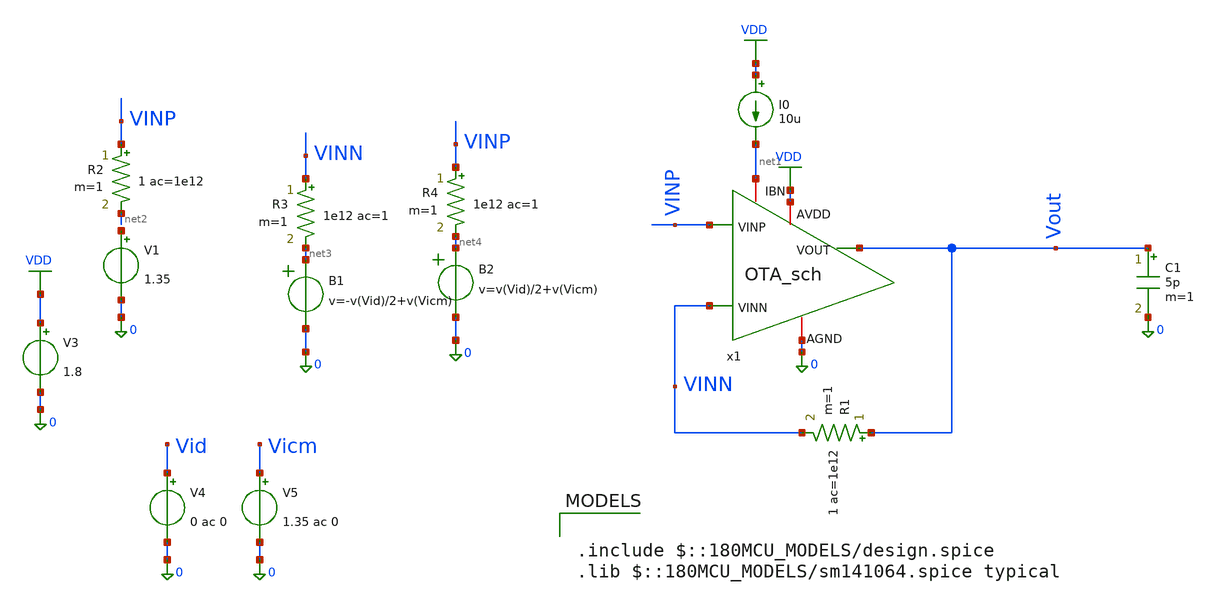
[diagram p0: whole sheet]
** sch_path: Lab_07/OTA_dc_cl_ac_ol.sch
**.subckt OTA_dc_cl_ac_ol
x1 VINP VDD VINN net1 0 Vout OTA_sch
V3 VDD 0 1.8
I0 VDD net1 10u
V1 net5 0 1.35
V4 Vid 0 0 ac 0
V5 Vicm 0 1.35 ac 0
B1 net3 0 v=-v(Vid)/2+v(Vicm)
B2 net4 0 v=v(Vid)/2+v(Vicm)
C1 Vout 0 5p m=1
R1 Vout VINN 1 ac=1e12 m=1
R4 VINP net4 1e12 ac=1 m=1
R3 VINN net3 1e12 ac=1 m=1
R2 VINP net2 1 ac=1e12 m=1
**** begin user architecture code

.include $::180MCU_MODELS/design.spice
.lib $::180MCU_MODELS/sm141064.spice typical


.control
alterparam sw_stat_global = 0
alterparam sw_stat_mismatch = 0
reset
save all
save @m.x1.xm1.m0[id]
save @m.x1.xm2.m0[id]
let index = 0
compose VICM_vec start=0.8 stop=1.5 step=50m
let Avcm_vec = VICM_vec
let id1_vec = VICM_vec
let id2_vec = VICM_vec
setscale VICM_vec
foreach VICM_val $&VICM_vec
alter V5 $VICM_val
op
let id1_vec[index] = @m.x1.xm1.m0[id]
let id2_vec[index] = @m.x1.xm2.m0[id]
* === COMMON MODE AC ===
alter V4 AC = 0
alter V5 AC = 1
ac dec 10 1 10e9
* === MEASUREMENTS ===
meas ac Av_CM_mag find vmag(VOUT) at=1
let Avcm_vec[index] = Av_CM_mag
let index = index + 1
end
write 5t_ota_tb_dc_cl_ac_ol.raw Avcm_vec id1_vec id2_vec
plot Avcm_vec vs VICM_vec
plot id1_vec id2_vec vs VICM_vec
.endc

**** end user architecture code
**.ends

* expanding   symbol:  OTA_sch.sym # of pins=6
** sym_path: Lab_07/OTA_sch.sym
** sch_path: Lab_07/OTA_sch.sch
.subckt OTA_sch VINP AVDD VINN IBN AGND VOUT
*.iopin AVDD
*.iopin IBN
*.iopin AGND
*.opin VOUT
*.ipin VINN
*.ipin VINP
XM1 net1 VINP net2 AGND nfet_03v3 L=450n W=8.237u nf=1 ad='int((nf+1)/2) * W/nf * 0.18u' as='int((nf+2)/2) * W/nf * 0.18u'
+ pd='2*int((nf+1)/2) * (W/nf + 0.18u)' ps='2*int((nf+2)/2) * (W/nf + 0.18u)' nrd='0.18u / W' nrs='0.18u / W'
+ sa=0 sb=0 sd=0 m=1
XM2 VOUT VINN net2 AGND nfet_03v3 L=450n W=8.237u nf=1 ad='int((nf+1)/2) * W/nf * 0.18u' as='int((nf+2)/2) * W/nf * 0.18u'
+ pd='2*int((nf+1)/2) * (W/nf + 0.18u)' ps='2*int((nf+2)/2) * (W/nf + 0.18u)' nrd='0.18u / W' nrs='0.18u / W'
+ sa=0 sb=0 sd=0 m=1
XM3 net2 IBN AGND AGND nfet_03v3 L=1u W=4.64*2u nf=1 ad='int((nf+1)/2) * W/nf * 0.18u' as='int((nf+2)/2) * W/nf * 0.18u'
+ pd='2*int((nf+1)/2) * (W/nf + 0.18u)' ps='2*int((nf+2)/2) * (W/nf + 0.18u)' nrd='0.18u / W' nrs='0.18u / W'
+ sa=0 sb=0 sd=0 m=1
XM4 IBN IBN AGND AGND nfet_03v3 L=1u W=4.64u nf=1 ad='int((nf+1)/2) * W/nf * 0.18u' as='int((nf+2)/2) * W/nf * 0.18u'
+ pd='2*int((nf+1)/2) * (W/nf + 0.18u)' ps='2*int((nf+2)/2) * (W/nf + 0.18u)' nrd='0.18u / W' nrs='0.18u / W'
+ sa=0 sb=0 sd=0 m=1
XM5 net1 net1 AVDD AVDD pfet_03v3 L=450n W=7.52u nf=1 ad='int((nf+1)/2) * W/nf * 0.18u' as='int((nf+2)/2) * W/nf * 0.18u'
+ pd='2*int((nf+1)/2) * (W/nf + 0.18u)' ps='2*int((nf+2)/2) * (W/nf + 0.18u)' nrd='0.18u / W' nrs='0.18u / W'
+ sa=0 sb=0 sd=0 m=1
XM6 VOUT net1 AVDD AVDD pfet_03v3 L=450n W=7.52u nf=1 ad='int((nf+1)/2) * W/nf * 0.18u' as='int((nf+2)/2) * W/nf * 0.18u'
+ pd='2*int((nf+1)/2) * (W/nf + 0.18u)' ps='2*int((nf+2)/2) * (W/nf + 0.18u)' nrd='0.18u / W' nrs='0.18u / W'
+ sa=0 sb=0 sd=0 m=1
.ends

.GLOBAL VDD
.end
